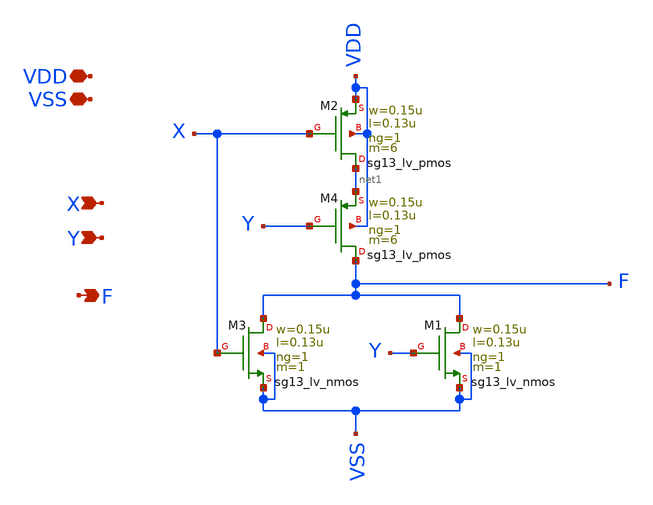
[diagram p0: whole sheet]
** sch_path: xschem/DigitalGates/NOR.sch
**.subckt NOR VDD X F VSS Y
*.iopin VDD
*.ipin X
*.opin F
*.iopin VSS
*.ipin Y
XM4 F Y net1 VDD sg13_lv_pmos w=0.15u l=0.13u ng=1 m=6 mm_ok=1
XM3 F X VSS VSS sg13_lv_nmos w=0.15u l=0.13u ng=1 m=1 mm_ok=1
XM1 F Y VSS VSS sg13_lv_nmos w=0.15u l=0.13u ng=1 m=1 mm_ok=1
XM2 net1 X VDD VDD sg13_lv_pmos w=0.15u l=0.13u ng=1 m=6 mm_ok=1
**** begin user architecture code



**** end user architecture code
**.ends
.end
